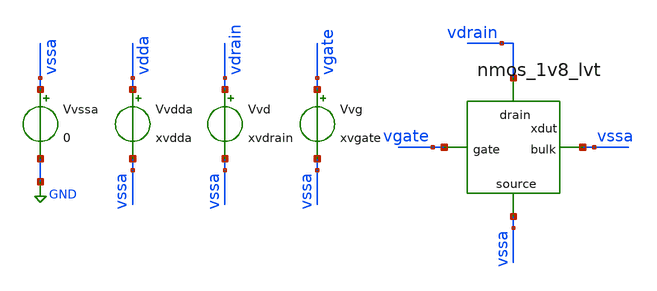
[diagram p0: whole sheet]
** sch_path: MC_analysys_single_corner/tb_mc_nmos.sch
**.subckt tb_mc_nmos
Vvdda vdda vssa xvdda
Vvssa vssa GND 0
Vvd vdrain vssa xvdrain
Vvg vgate vssa xvgate
xdut vdrain vssa vgate vssa nmos_1v8_lvt
**** begin user architecture code

** opencircuitdesign pdks install
*.lib $::SKYWATER_MODELS/sky130.lib.spice tt
*.lib /home/slice/pdk/SW130/share/pdk/sky130A/libs.tech/combined/sky130.lib.spice tt
.lib /home/slice/pdk/SW130/share/pdk/sky130A/libs.tech/combined/sky130.lib.spice tt_mm
*.lib /home/slice/pdk/SW130/share/pdk/sky130A/libs.tech/combined/sky130.lib.spice ss
*.lib /home/slice/pdk/SW130/share/pdk/sky130A/libs.tech/combined/sky130.lib.spice ff
*.lib /home/slice/pdk/SW130/share/pdk/sky130A/libs.tech/combined/sky130.lib.spice sf
*.lib /home/slice/pdk/SW130/share/pdk/sky130A/libs.tech/combined/sky130.lib.spice fs

* Parameters
.param xvdda = 1.8
.csparam xvdda_var = 'xvdda'
.param xvdrain = 1
.param xvgate = 1
.temp 27

  ** 1. DCOP analysis **
  ** must save the below for DCOP analysis to be back annotated onto the schematic
  .option savecurrents
  .save

  * svt device
  +  @m.xdut.xm1.msky130_fd_pr__nfet_01v8[vgs]
  +  @m.xdut.xm1.msky130_fd_pr__nfet_01v8[vds]
  +  @m.xdut.xm1.msky130_fd_pr__nfet_01v8[vth]
  +  @m.xdut.xm1.msky130_fd_pr__nfet_01v8[gds]
  +  @m.xdut.xm1.msky130_fd_pr__nfet_01v8[gm]
  +  @m.xdut.xm1.msky130_fd_pr__nfet_01v8[id]
  +  @m.xdut.xm1.msky130_fd_pr__nfet_01v8[vdsat]
  * hvt device
  +  @m.xdut.xm1.msky130_fd_pr__nfet_01v8_hvt[vgs]
  +  @m.xdut.xm1.msky130_fd_pr__nfet_01v8_hvt[vds]
  +  @m.xdut.xm1.msky130_fd_pr__nfet_01v8_hvt[vth]
  +  @m.xdut.xm1.msky130_fd_pr__nfet_01v8_hvt[gds]
  +  @m.xdut.xm1.msky130_fd_pr__nfet_01v8_hvt[gm]
  +  @m.xdut.xm1.msky130_fd_pr__nfet_01v8_hvt[id]
  +  @m.xdut.xm1.msky130_fd_pr__nfet_01v8_hvt[vdsat]
  * lvt device
  +  @m.xdut.xm1.msky130_fd_pr__nfet_01v8_lvt[vgs]
  +  @m.xdut.xm1.msky130_fd_pr__nfet_01v8_lvt[vds]
  +  @m.xdut.xm1.msky130_fd_pr__nfet_01v8_lvt[vth]
  +  @m.xdut.xm1.msky130_fd_pr__nfet_01v8_lvt[gds]
  +  @m.xdut.xm1.msky130_fd_pr__nfet_01v8_lvt[gm]
  +  @m.xdut.xm1.msky130_fd_pr__nfet_01v8_lvt[id]
  +  @m.xdut.xm1.msky130_fd_pr__nfet_01v8_lvt[vdsat]

  .control


    save all

    let run = 1

    dowhile run <= 200
    reset

    ** 1. DCOP ANALYSIS **
    op
    *let vth_meas = @m.xdut.xm1.msky130_fd_pr__nfet_01v8[vth]
    let vth_meas = @m.xdut.xm1.msky130_fd_pr__nfet_01v8_lvt[vth]
    *let vth_meas = @m.xdut.xm1.msky130_fd_pr__nfet_01v8_hvt[vth]
    echo "$&vth_meas" >> vth_measures.txt
    remzerovec
    * need to set appendwrite to accumulate the vth's from all runs
    * in one file. THIS MEANS YOU MUST ENSURE FILE "vth_measures.txt" IS
    * DELETED FROM THE RUNDIR PRIOR TO RUNNING THIS LOOP. Otherwise
    * MC data from an older analysis will corrupt the results from your
    * current analysis. For best practice you should also delete file
    * "tb_MC_PMOS.raw" to save diskspace.
    set appendwrite
    set filetype=ascii
    write tb_MC_NMOS.raw
    * release the memory holding the output data sets (good memory management)
    destroy all
    let run = run+1
    end

  setplot

quit 0
.endc




**** end user architecture code
**.ends

* expanding   symbol:  nmos_1v8_lvt.sym # of pins=4
** sym_path: MC_analysys_single_corner/DUT.sym
** sch_path: MC_analysys_single_corner/nmos_1v8_lvt.sch
.subckt nmos_1v8_lvt drain bulk gate source
*.ipin gate
*.opin drain
*.ipin bulk
*.ipin source
XM1 drain gate source bulk sky130_fd_pr__nfet_01v8_lvt L=2 W=0.625 nf=1 ad='int((nf+1)/2) * W/nf * 0.29' as='int((nf+2)/2)
+ * W/nf * 0.29' pd='2*int((nf+1)/2) * (W/nf + 0.29)' ps='2*int((nf+2)/2) * (W/nf + 0.29)' nrd='0.29 /
+ W' nrs='0.29 / W' sa=0 sb=0 sd=0 mult=1 m=1
.ends

.GLOBAL GND
.end
